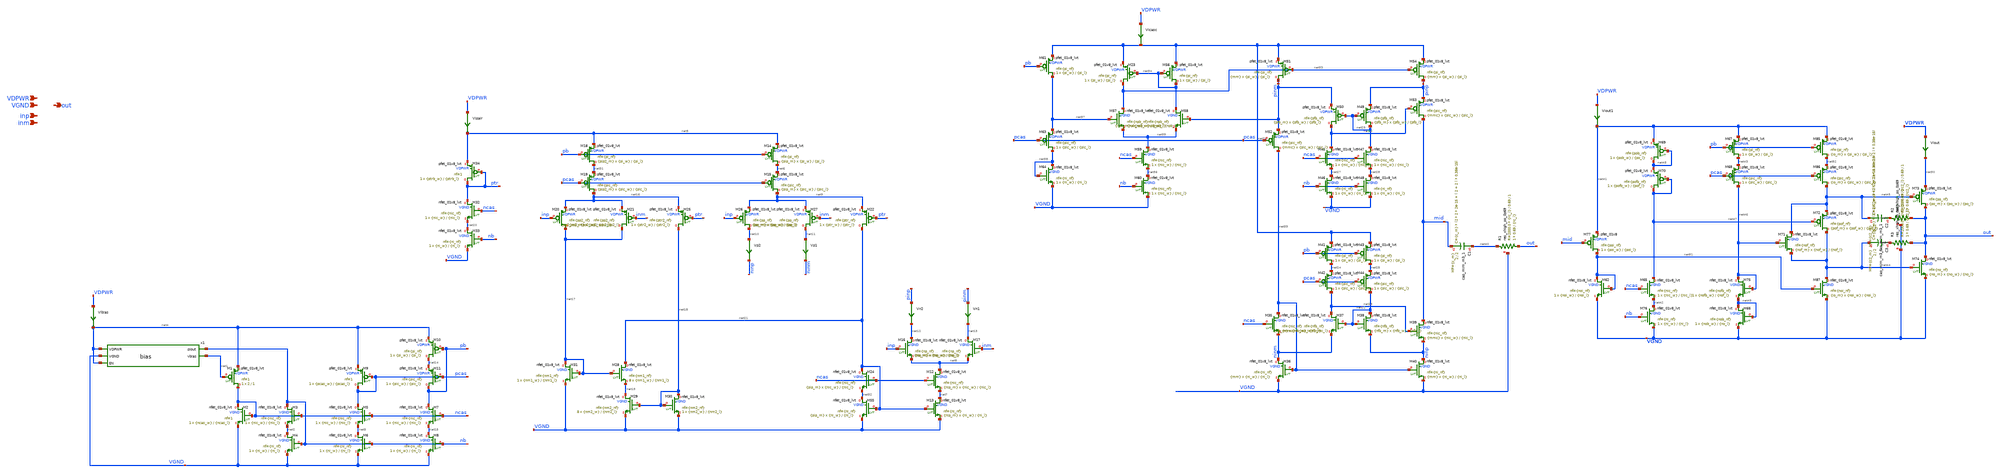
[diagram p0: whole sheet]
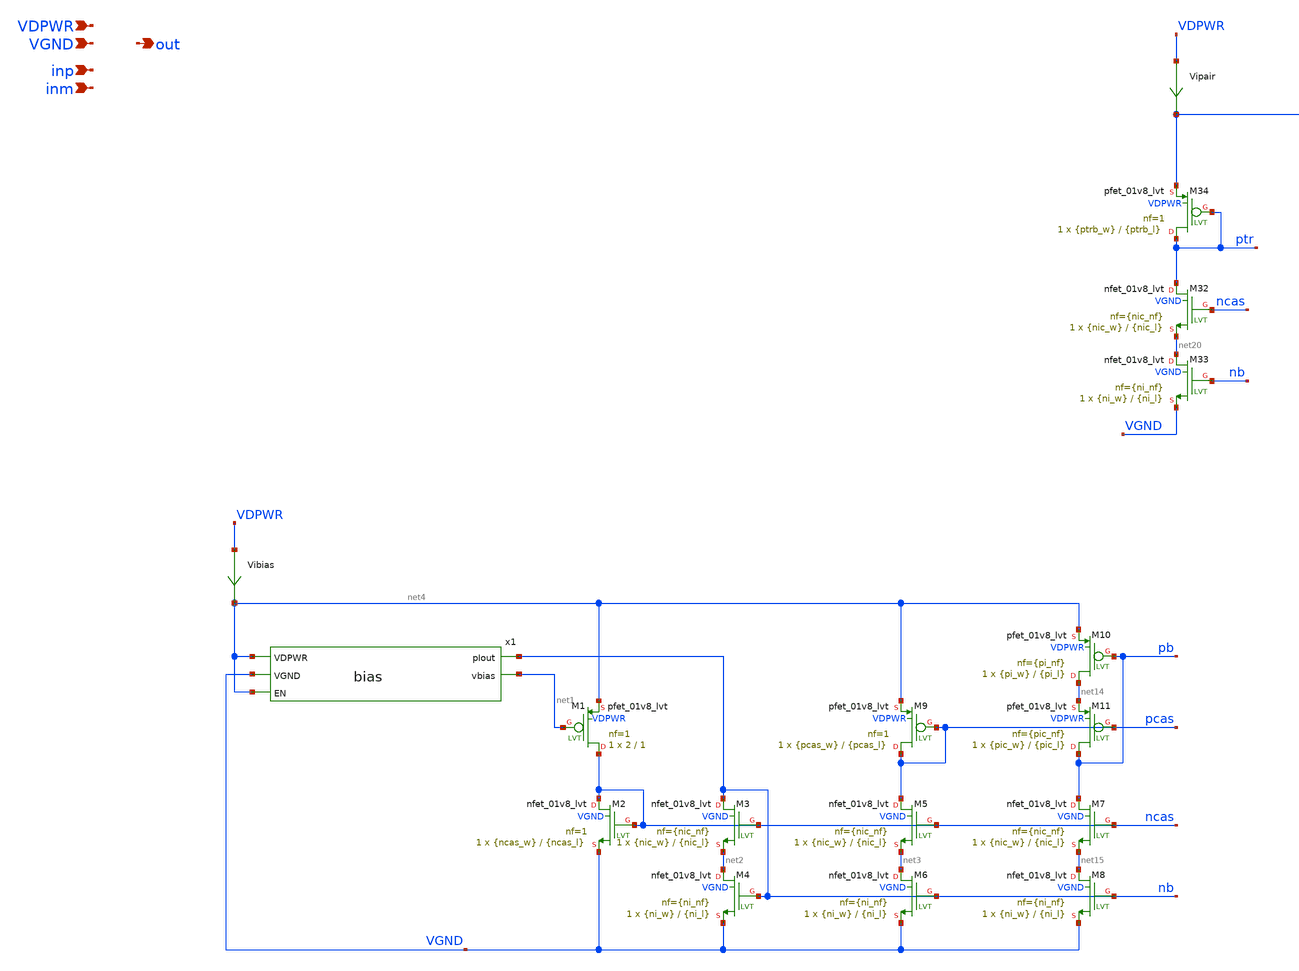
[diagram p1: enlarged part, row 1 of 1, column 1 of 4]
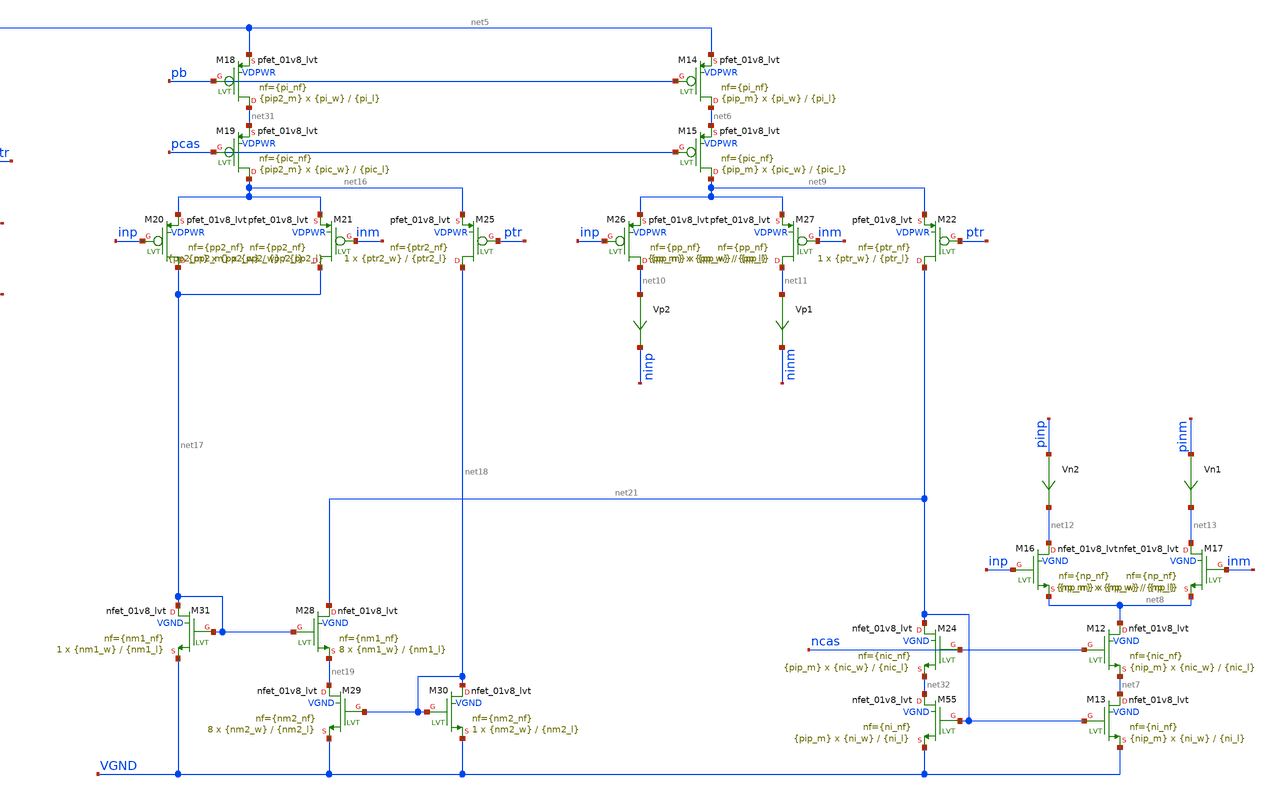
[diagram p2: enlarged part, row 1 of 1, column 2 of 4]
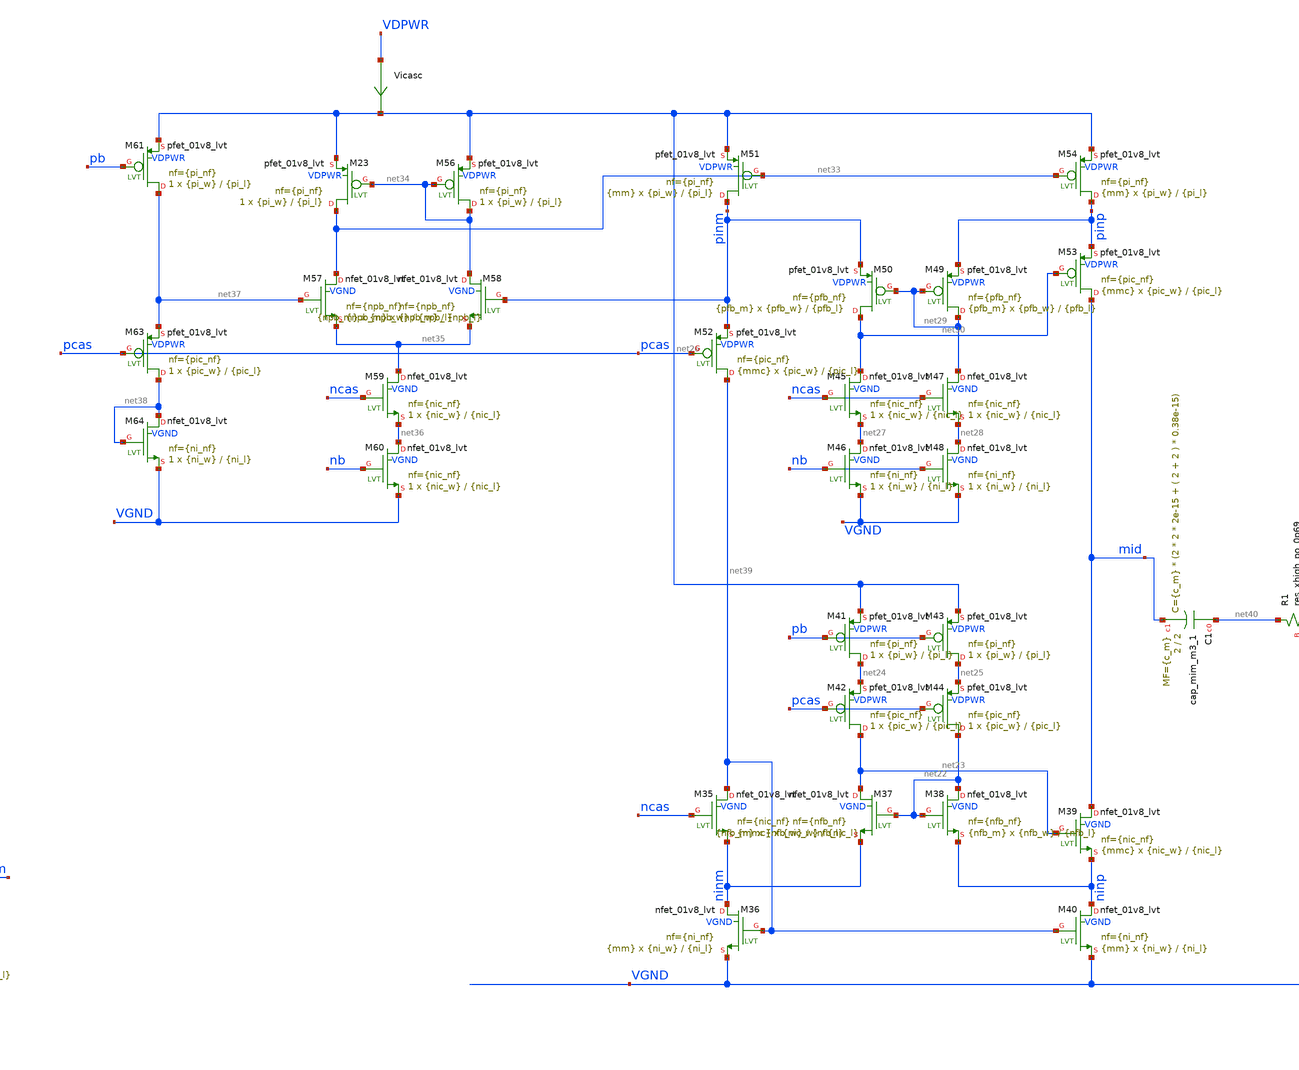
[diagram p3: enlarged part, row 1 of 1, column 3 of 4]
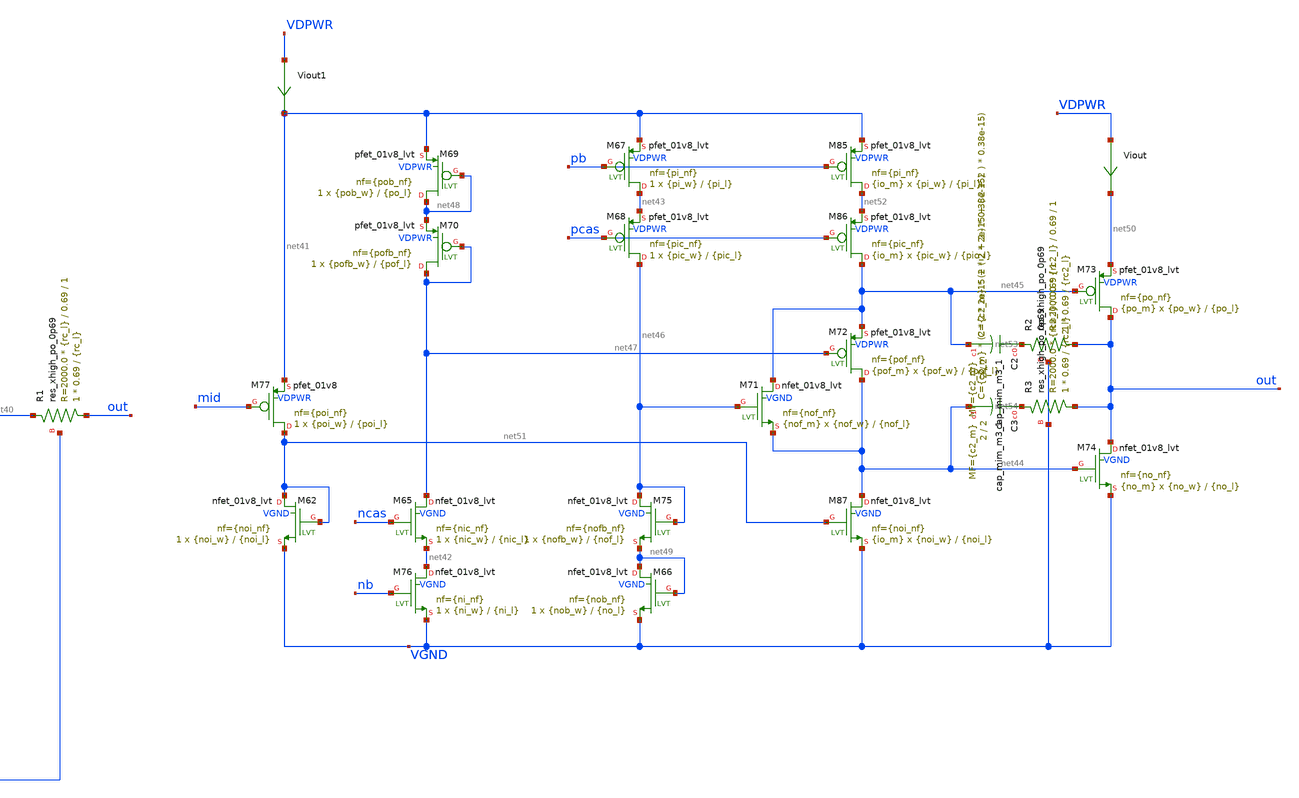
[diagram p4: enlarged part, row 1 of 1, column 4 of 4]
** sch_path: xschem/opamp_testing2.sch
**.subckt opamp_testing2 VDPWR VGND inp inm out
*.ipin VDPWR
*.ipin VGND
*.ipin inp
*.ipin inm
*.opin out
x1 net4 nb VGND net4 net1 bias
XM1 ncas net1 net4 VDPWR sky130_fd_pr__pfet_01v8_lvt L=1 W=2 nf=1 ad='int((1 + 1)/2) * 2 / 1 * 0.29'
+ as='int((1 + 2)/2) * 2 / 1 * 0.29' pd='2*int((1 + 1)/2) * (2 / 1 + 0.29)' ps='2*int((1 + 2)/2) * (2 / 1 + 0.29)'
+ nrd='0.29 / 2 ' nrs='0.29 / 2 ' sa=0 sb=0 sd=0 mult=1 m=1
XM2 ncas ncas VGND VGND sky130_fd_pr__nfet_01v8_lvt L={ncas_l} W={ncas_w} nf=1 ad='int((1 + 1)/2) * {ncas_w} / 1 * 0.29'
+ as='int((1 + 2)/2) * {ncas_w} / 1 * 0.29' pd='2*int((1 + 1)/2) * ({ncas_w} / 1 + 0.29)' ps='2*int((1 + 2)/2) * ({ncas_w} / 1 + 0.29)'
+ nrd='0.29 / {ncas_w} ' nrs='0.29 / {ncas_w} ' sa=0 sb=0 sd=0 mult=1 m=1
XM3 nb ncas net2 VGND sky130_fd_pr__nfet_01v8_lvt L={nic_l} W={nic_w} nf={nic_nf} ad='int(({nic_nf} + 1)/2) * {nic_w} / {nic_nf} * 0.29'
+ as='int(({nic_nf} + 2)/2) * {nic_w} / {nic_nf} * 0.29' pd='2*int(({nic_nf} + 1)/2) * ({nic_w} / {nic_nf} + 0.29)'
+ ps='2*int(({nic_nf} + 2)/2) * ({nic_w} / {nic_nf} + 0.29)' nrd='0.29 / {nic_w} ' nrs='0.29 / {nic_w} '
+ sa=0 sb=0 sd=0 mult=1 m=1
XM4 net2 nb VGND VGND sky130_fd_pr__nfet_01v8_lvt L={ni_l} W={ni_w} nf={ni_nf} ad='int(({ni_nf} + 1)/2) * {ni_w} / {ni_nf} * 0.29'
+ as='int(({ni_nf} + 2)/2) * {ni_w} / {ni_nf} * 0.29' pd='2*int(({ni_nf} + 1)/2) * ({ni_w} / {ni_nf} + 0.29)'
+ ps='2*int(({ni_nf} + 2)/2) * ({ni_w} / {ni_nf} + 0.29)' nrd='0.29 / {ni_w} ' nrs='0.29 / {ni_w} ' sa=0
+ sb=0 sd=0 mult=1 m=1
XM5 pcas ncas net3 VGND sky130_fd_pr__nfet_01v8_lvt L={nic_l} W={nic_w} nf={nic_nf} ad='int(({nic_nf} + 1)/2) * {nic_w} / {nic_nf} * 0.29'
+ as='int(({nic_nf} + 2)/2) * {nic_w} / {nic_nf} * 0.29' pd='2*int(({nic_nf} + 1)/2) * ({nic_w} / {nic_nf} + 0.29)'
+ ps='2*int(({nic_nf} + 2)/2) * ({nic_w} / {nic_nf} + 0.29)' nrd='0.29 / {nic_w} ' nrs='0.29 / {nic_w} '
+ sa=0 sb=0 sd=0 mult=1 m=1
XM6 net3 nb VGND VGND sky130_fd_pr__nfet_01v8_lvt L={ni_l} W={ni_w} nf={ni_nf} ad='int(({ni_nf} + 1)/2) * {ni_w} / {ni_nf} * 0.29'
+ as='int(({ni_nf} + 2)/2) * {ni_w} / {ni_nf} * 0.29' pd='2*int(({ni_nf} + 1)/2) * ({ni_w} / {ni_nf} + 0.29)'
+ ps='2*int(({ni_nf} + 2)/2) * ({ni_w} / {ni_nf} + 0.29)' nrd='0.29 / {ni_w} ' nrs='0.29 / {ni_w} ' sa=0
+ sb=0 sd=0 mult=1 m=1
XM7 pb ncas net15 VGND sky130_fd_pr__nfet_01v8_lvt L={nic_l} W={nic_w} nf={nic_nf} ad='int(({nic_nf} + 1)/2) * {nic_w} / {nic_nf} * 0.29'
+ as='int(({nic_nf} + 2)/2) * {nic_w} / {nic_nf} * 0.29' pd='2*int(({nic_nf} + 1)/2) * ({nic_w} / {nic_nf} + 0.29)'
+ ps='2*int(({nic_nf} + 2)/2) * ({nic_w} / {nic_nf} + 0.29)' nrd='0.29 / {nic_w} ' nrs='0.29 / {nic_w} '
+ sa=0 sb=0 sd=0 mult=1 m=1
XM8 net15 nb VGND VGND sky130_fd_pr__nfet_01v8_lvt L={ni_l} W={ni_w} nf={ni_nf} ad='int(({ni_nf} + 1)/2) * {ni_w} / {ni_nf} * 0.29'
+ as='int(({ni_nf} + 2)/2) * {ni_w} / {ni_nf} * 0.29' pd='2*int(({ni_nf} + 1)/2) * ({ni_w} / {ni_nf} + 0.29)'
+ ps='2*int(({ni_nf} + 2)/2) * ({ni_w} / {ni_nf} + 0.29)' nrd='0.29 / {ni_w} ' nrs='0.29 / {ni_w} ' sa=0
+ sb=0 sd=0 mult=1 m=1
XM9 pcas pcas net4 VDPWR sky130_fd_pr__pfet_01v8_lvt L={pcas_l} W={pcas_w} nf=1 ad='int((1 + 1)/2) * {pcas_w} / 1 * 0.29'
+ as='int((1 + 2)/2) * {pcas_w} / 1 * 0.29' pd='2*int((1 + 1)/2) * ({pcas_w} / 1 + 0.29)' ps='2*int((1 + 2)/2) * ({pcas_w} / 1 + 0.29)'
+ nrd='0.29 / {pcas_w} ' nrs='0.29 / {pcas_w} ' sa=0 sb=0 sd=0 mult=1 m=1
XM10 net14 pb net4 VDPWR sky130_fd_pr__pfet_01v8_lvt L={pi_l} W={pi_w} nf={pi_nf} ad='int(({pi_nf} + 1)/2) * {pi_w} / {pi_nf} * 0.29'
+ as='int(({pi_nf} + 2)/2) * {pi_w} / {pi_nf} * 0.29' pd='2*int(({pi_nf} + 1)/2) * ({pi_w} / {pi_nf} + 0.29)'
+ ps='2*int(({pi_nf} + 2)/2) * ({pi_w} / {pi_nf} + 0.29)' nrd='0.29 / {pi_w} ' nrs='0.29 / {pi_w} ' sa=0
+ sb=0 sd=0 mult=1 m=1
XM11 pb pcas net14 VDPWR sky130_fd_pr__pfet_01v8_lvt L={pic_l} W={pic_w} nf={pic_nf} ad='int(({pic_nf} + 1)/2) * {pic_w} / {pic_nf} * 0.29'
+ as='int(({pic_nf} + 2)/2) * {pic_w} / {pic_nf} * 0.29' pd='2*int(({pic_nf} + 1)/2) * ({pic_w} / {pic_nf} + 0.29)'
+ ps='2*int(({pic_nf} + 2)/2) * ({pic_w} / {pic_nf} + 0.29)' nrd='0.29 / {pic_w} ' nrs='0.29 / {pic_w} '
+ sa=0 sb=0 sd=0 mult=1 m=1
XM12 net8 ncas net7 VGND sky130_fd_pr__nfet_01v8_lvt L={nic_l} W={nic_w} nf={nic_nf} ad='int(({nic_nf} + 1)/2) * {nic_w} / {nic_nf} * 0.29'
+ as='int(({nic_nf} + 2)/2) * {nic_w} / {nic_nf} * 0.29' pd='2*int(({nic_nf} + 1)/2) * ({nic_w} / {nic_nf} + 0.29)'
+ ps='2*int(({nic_nf} + 2)/2) * ({nic_w} / {nic_nf} + 0.29)' nrd='0.29 / {nic_w} ' nrs='0.29 / {nic_w} '
+ sa=0 sb=0 sd=0 mult={nip_m} m={nip_m}
XM13 net7 net21 VGND VGND sky130_fd_pr__nfet_01v8_lvt L={ni_l} W={ni_w} nf={ni_nf} ad='int(({ni_nf} + 1)/2) * {ni_w} / {ni_nf} * 0.29'
+ as='int(({ni_nf} + 2)/2) * {ni_w} / {ni_nf} * 0.29' pd='2*int(({ni_nf} + 1)/2) * ({ni_w} / {ni_nf} + 0.29)'
+ ps='2*int(({ni_nf} + 2)/2) * ({ni_w} / {ni_nf} + 0.29)' nrd='0.29 / {ni_w} ' nrs='0.29 / {ni_w} ' sa=0
+ sb=0 sd=0 mult={nip_m} m={nip_m}
XM14 net6 pb net5 VDPWR sky130_fd_pr__pfet_01v8_lvt L={pi_l} W={pi_w} nf={pi_nf} ad='int(({pi_nf} + 1)/2) * {pi_w} / {pi_nf} * 0.29'
+ as='int(({pi_nf} + 2)/2) * {pi_w} / {pi_nf} * 0.29' pd='2*int(({pi_nf} + 1)/2) * ({pi_w} / {pi_nf} + 0.29)'
+ ps='2*int(({pi_nf} + 2)/2) * ({pi_w} / {pi_nf} + 0.29)' nrd='0.29 / {pi_w} ' nrs='0.29 / {pi_w} ' sa=0
+ sb=0 sd=0 mult={pip_m} m={pip_m}
XM15 net9 pcas net6 VDPWR sky130_fd_pr__pfet_01v8_lvt L={pic_l} W={pic_w} nf={pic_nf} ad='int(({pic_nf} + 1)/2) * {pic_w} / {pic_nf} * 0.29'
+ as='int(({pic_nf} + 2)/2) * {pic_w} / {pic_nf} * 0.29' pd='2*int(({pic_nf} + 1)/2) * ({pic_w} / {pic_nf} + 0.29)'
+ ps='2*int(({pic_nf} + 2)/2) * ({pic_w} / {pic_nf} + 0.29)' nrd='0.29 / {pic_w} ' nrs='0.29 / {pic_w} '
+ sa=0 sb=0 sd=0 mult={pip_m} m={pip_m}
XM16 net12 inp net8 VGND sky130_fd_pr__nfet_01v8_lvt L={np_l} W={np_w} nf={np_nf} ad='int(({np_nf} + 1)/2) * {np_w} / {np_nf} * 0.29'
+ as='int(({np_nf} + 2)/2) * {np_w} / {np_nf} * 0.29' pd='2*int(({np_nf} + 1)/2) * ({np_w} / {np_nf} + 0.29)'
+ ps='2*int(({np_nf} + 2)/2) * ({np_w} / {np_nf} + 0.29)' nrd='0.29 / {np_w} ' nrs='0.29 / {np_w} ' sa=0
+ sb=0 sd=0 mult={np_m} m={np_m}
XM17 net13 inm net8 VGND sky130_fd_pr__nfet_01v8_lvt L={np_l} W={np_w} nf={np_nf} ad='int(({np_nf} + 1)/2) * {np_w} / {np_nf} * 0.29'
+ as='int(({np_nf} + 2)/2) * {np_w} / {np_nf} * 0.29' pd='2*int(({np_nf} + 1)/2) * ({np_w} / {np_nf} + 0.29)'
+ ps='2*int(({np_nf} + 2)/2) * ({np_w} / {np_nf} + 0.29)' nrd='0.29 / {np_w} ' nrs='0.29 / {np_w} ' sa=0
+ sb=0 sd=0 mult={np_m} m={np_m}
XM26 net10 inp net9 VDPWR sky130_fd_pr__pfet_01v8_lvt L={pp_l} W={pp_w} nf={pp_nf} ad='int(({pp_nf} + 1)/2) * {pp_w} / {pp_nf} * 0.29'
+ as='int(({pp_nf} + 2)/2) * {pp_w} / {pp_nf} * 0.29' pd='2*int(({pp_nf} + 1)/2) * ({pp_w} / {pp_nf} + 0.29)'
+ ps='2*int(({pp_nf} + 2)/2) * ({pp_w} / {pp_nf} + 0.29)' nrd='0.29 / {pp_w} ' nrs='0.29 / {pp_w} ' sa=0
+ sb=0 sd=0 mult={pp_m} m={pp_m}
XM27 net11 inm net9 VDPWR sky130_fd_pr__pfet_01v8_lvt L={pp_l} W={pp_w} nf={pp_nf} ad='int(({pp_nf} + 1)/2) * {pp_w} / {pp_nf} * 0.29'
+ as='int(({pp_nf} + 2)/2) * {pp_w} / {pp_nf} * 0.29' pd='2*int(({pp_nf} + 1)/2) * ({pp_w} / {pp_nf} + 0.29)'
+ ps='2*int(({pp_nf} + 2)/2) * ({pp_w} / {pp_nf} + 0.29)' nrd='0.29 / {pp_w} ' nrs='0.29 / {pp_w} ' sa=0
+ sb=0 sd=0 mult={pp_m} m={pp_m}
Vp1 net11 ninm 0
.save i(vp1)
Vp2 net10 ninp 0
.save i(vp2)
Vn1 pinm net13 0
.save i(vn1)
Vn2 pinp net12 0
.save i(vn2)
XM18 net31 pb net5 VDPWR sky130_fd_pr__pfet_01v8_lvt L={pi_l} W={pi_w} nf={pi_nf} ad='int(({pi_nf} + 1)/2) * {pi_w} / {pi_nf} * 0.29'
+ as='int(({pi_nf} + 2)/2) * {pi_w} / {pi_nf} * 0.29' pd='2*int(({pi_nf} + 1)/2) * ({pi_w} / {pi_nf} + 0.29)'
+ ps='2*int(({pi_nf} + 2)/2) * ({pi_w} / {pi_nf} + 0.29)' nrd='0.29 / {pi_w} ' nrs='0.29 / {pi_w} ' sa=0
+ sb=0 sd=0 mult={pip2_m} m={pip2_m}
XM19 net16 pcas net31 VDPWR sky130_fd_pr__pfet_01v8_lvt L={pic_l} W={pic_w} nf={pic_nf} ad='int(({pic_nf} + 1)/2) * {pic_w} / {pic_nf} * 0.29'
+ as='int(({pic_nf} + 2)/2) * {pic_w} / {pic_nf} * 0.29' pd='2*int(({pic_nf} + 1)/2) * ({pic_w} / {pic_nf} + 0.29)'
+ ps='2*int(({pic_nf} + 2)/2) * ({pic_w} / {pic_nf} + 0.29)' nrd='0.29 / {pic_w} ' nrs='0.29 / {pic_w} '
+ sa=0 sb=0 sd=0 mult={pip2_m} m={pip2_m}
XM20 net17 inp net16 VDPWR sky130_fd_pr__pfet_01v8_lvt L={pp2_l} W={pp2_w} nf={pp2_nf} ad='int(({pp2_nf} + 1)/2) * {pp2_w} / {pp2_nf} * 0.29'
+ as='int(({pp2_nf} + 2)/2) * {pp2_w} / {pp2_nf} * 0.29' pd='2*int(({pp2_nf} + 1)/2) * ({pp2_w} / {pp2_nf} + 0.29)'
+ ps='2*int(({pp2_nf} + 2)/2) * ({pp2_w} / {pp2_nf} + 0.29)' nrd='0.29 / {pp2_w} ' nrs='0.29 / {pp2_w} '
+ sa=0 sb=0 sd=0 mult={pp2_m} m={pp2_m}
XM21 net17 inm net16 VDPWR sky130_fd_pr__pfet_01v8_lvt L={pp2_l} W={pp2_w} nf={pp2_nf} ad='int(({pp2_nf} + 1)/2) * {pp2_w} / {pp2_nf} * 0.29'
+ as='int(({pp2_nf} + 2)/2) * {pp2_w} / {pp2_nf} * 0.29' pd='2*int(({pp2_nf} + 1)/2) * ({pp2_w} / {pp2_nf} + 0.29)'
+ ps='2*int(({pp2_nf} + 2)/2) * ({pp2_w} / {pp2_nf} + 0.29)' nrd='0.29 / {pp2_w} ' nrs='0.29 / {pp2_w} '
+ sa=0 sb=0 sd=0 mult={pp2_m} m={pp2_m}
XM25 net18 ptr net16 VDPWR sky130_fd_pr__pfet_01v8_lvt L={ptr2_l} W={ptr2_w} nf={ptr2_nf} ad='int(({ptr2_nf} + 1)/2) * {ptr2_w} / {ptr2_nf} * 0.29'
+ as='int(({ptr2_nf} + 2)/2) * {ptr2_w} / {ptr2_nf} * 0.29' pd='2*int(({ptr2_nf} + 1)/2) * ({ptr2_w} / {ptr2_nf} + 0.29)'
+ ps='2*int(({ptr2_nf} + 2)/2) * ({ptr2_w} / {ptr2_nf} + 0.29)' nrd='0.29 / {ptr2_w} ' nrs='0.29 / {ptr2_w} '
+ sa=0 sb=0 sd=0 mult=1 m=1
XM28 net21 net17 net19 VGND sky130_fd_pr__nfet_01v8_lvt L={nm1_l} W={nm1_w} nf={nm1_nf} ad='int(({nm1_nf} + 1)/2) * {nm1_w} / {nm1_nf} * 0.29'
+ as='int(({nm1_nf} + 2)/2) * {nm1_w} / {nm1_nf} * 0.29' pd='2*int(({nm1_nf} + 1)/2) * ({nm1_w} / {nm1_nf} + 0.29)'
+ ps='2*int(({nm1_nf} + 2)/2) * ({nm1_w} / {nm1_nf} + 0.29)' nrd='0.29 / {nm1_w} ' nrs='0.29 / {nm1_w} '
+ sa=0 sb=0 sd=0 mult=8 m=8
XM29 net19 net18 VGND VGND sky130_fd_pr__nfet_01v8_lvt L={nm2_l} W={nm2_w} nf={nm2_nf} ad='int(({nm2_nf} + 1)/2) * {nm2_w} / {nm2_nf} * 0.29'
+ as='int(({nm2_nf} + 2)/2) * {nm2_w} / {nm2_nf} * 0.29' pd='2*int(({nm2_nf} + 1)/2) * ({nm2_w} / {nm2_nf} + 0.29)'
+ ps='2*int(({nm2_nf} + 2)/2) * ({nm2_w} / {nm2_nf} + 0.29)' nrd='0.29 / {nm2_w} ' nrs='0.29 / {nm2_w} '
+ sa=0 sb=0 sd=0 mult=8 m=8
XM30 net18 net18 VGND VGND sky130_fd_pr__nfet_01v8_lvt L={nm2_l} W={nm2_w} nf={nm2_nf} ad='int(({nm2_nf} + 1)/2) * {nm2_w} / {nm2_nf} * 0.29'
+ as='int(({nm2_nf} + 2)/2) * {nm2_w} / {nm2_nf} * 0.29' pd='2*int(({nm2_nf} + 1)/2) * ({nm2_w} / {nm2_nf} + 0.29)'
+ ps='2*int(({nm2_nf} + 2)/2) * ({nm2_w} / {nm2_nf} + 0.29)' nrd='0.29 / {nm2_w} ' nrs='0.29 / {nm2_w} '
+ sa=0 sb=0 sd=0 mult=1 m=1
XM31 net17 net17 VGND VGND sky130_fd_pr__nfet_01v8_lvt L={nm1_l} W={nm1_w} nf={nm1_nf} ad='int(({nm1_nf} + 1)/2) * {nm1_w} / {nm1_nf} * 0.29'
+ as='int(({nm1_nf} + 2)/2) * {nm1_w} / {nm1_nf} * 0.29' pd='2*int(({nm1_nf} + 1)/2) * ({nm1_w} / {nm1_nf} + 0.29)'
+ ps='2*int(({nm1_nf} + 2)/2) * ({nm1_w} / {nm1_nf} + 0.29)' nrd='0.29 / {nm1_w} ' nrs='0.29 / {nm1_w} '
+ sa=0 sb=0 sd=0 mult=1 m=1
XM32 ptr ncas net20 VGND sky130_fd_pr__nfet_01v8_lvt L={nic_l} W={nic_w} nf={nic_nf} ad='int(({nic_nf} + 1)/2) * {nic_w} / {nic_nf} * 0.29'
+ as='int(({nic_nf} + 2)/2) * {nic_w} / {nic_nf} * 0.29' pd='2*int(({nic_nf} + 1)/2) * ({nic_w} / {nic_nf} + 0.29)'
+ ps='2*int(({nic_nf} + 2)/2) * ({nic_w} / {nic_nf} + 0.29)' nrd='0.29 / {nic_w} ' nrs='0.29 / {nic_w} '
+ sa=0 sb=0 sd=0 mult=1 m=1
XM33 net20 nb VGND VGND sky130_fd_pr__nfet_01v8_lvt L={ni_l} W={ni_w} nf={ni_nf} ad='int(({ni_nf} + 1)/2) * {ni_w} / {ni_nf} * 0.29'
+ as='int(({ni_nf} + 2)/2) * {ni_w} / {ni_nf} * 0.29' pd='2*int(({ni_nf} + 1)/2) * ({ni_w} / {ni_nf} + 0.29)'
+ ps='2*int(({ni_nf} + 2)/2) * ({ni_w} / {ni_nf} + 0.29)' nrd='0.29 / {ni_w} ' nrs='0.29 / {ni_w} ' sa=0
+ sb=0 sd=0 mult=1 m=1
XM34 ptr ptr net5 VDPWR sky130_fd_pr__pfet_01v8_lvt L={ptrb_l} W={ptrb_w} nf=1 ad='int((1 + 1)/2) * {ptrb_w} / 1 * 0.29'
+ as='int((1 + 2)/2) * {ptrb_w} / 1 * 0.29' pd='2*int((1 + 1)/2) * ({ptrb_w} / 1 + 0.29)' ps='2*int((1 + 2)/2) * ({ptrb_w} / 1 + 0.29)'
+ nrd='0.29 / {ptrb_w} ' nrs='0.29 / {ptrb_w} ' sa=0 sb=0 sd=0 mult=1 m=1
XM35 net39 ncas ninm VGND sky130_fd_pr__nfet_01v8_lvt L={nic_l} W={nic_w} nf={nic_nf} ad='int(({nic_nf} + 1)/2) * {nic_w} / {nic_nf} * 0.29'
+ as='int(({nic_nf} + 2)/2) * {nic_w} / {nic_nf} * 0.29' pd='2*int(({nic_nf} + 1)/2) * ({nic_w} / {nic_nf} + 0.29)'
+ ps='2*int(({nic_nf} + 2)/2) * ({nic_w} / {nic_nf} + 0.29)' nrd='0.29 / {nic_w} ' nrs='0.29 / {nic_w} '
+ sa=0 sb=0 sd=0 mult={mmc} m={mmc}
XM36 ninm net39 VGND VGND sky130_fd_pr__nfet_01v8_lvt L={ni_l} W={ni_w} nf={ni_nf} ad='int(({ni_nf} + 1)/2) * {ni_w} / {ni_nf} * 0.29'
+ as='int(({ni_nf} + 2)/2) * {ni_w} / {ni_nf} * 0.29' pd='2*int(({ni_nf} + 1)/2) * ({ni_w} / {ni_nf} + 0.29)'
+ ps='2*int(({ni_nf} + 2)/2) * ({ni_w} / {ni_nf} + 0.29)' nrd='0.29 / {ni_w} ' nrs='0.29 / {ni_w} ' sa=0
+ sb=0 sd=0 mult={mm} m={mm}
XM37 net23 net22 ninm VGND sky130_fd_pr__nfet_01v8_lvt L={nfb_l} W={nfb_w} nf={nfb_nf} ad='int(({nfb_nf} + 1)/2) * {nfb_w} / {nfb_nf} * 0.29'
+ as='int(({nfb_nf} + 2)/2) * {nfb_w} / {nfb_nf} * 0.29' pd='2*int(({nfb_nf} + 1)/2) * ({nfb_w} / {nfb_nf} + 0.29)'
+ ps='2*int(({nfb_nf} + 2)/2) * ({nfb_w} / {nfb_nf} + 0.29)' nrd='0.29 / {nfb_w} ' nrs='0.29 / {nfb_w} '
+ sa=0 sb=0 sd=0 mult={nfb_m} m={nfb_m}
XM39 mid net23 ninp VGND sky130_fd_pr__nfet_01v8_lvt L={nic_l} W={nic_w} nf={nic_nf} ad='int(({nic_nf} + 1)/2) * {nic_w} / {nic_nf} * 0.29'
+ as='int(({nic_nf} + 2)/2) * {nic_w} / {nic_nf} * 0.29' pd='2*int(({nic_nf} + 1)/2) * ({nic_w} / {nic_nf} + 0.29)'
+ ps='2*int(({nic_nf} + 2)/2) * ({nic_w} / {nic_nf} + 0.29)' nrd='0.29 / {nic_w} ' nrs='0.29 / {nic_w} '
+ sa=0 sb=0 sd=0 mult={mmc} m={mmc}
XM40 ninp net39 VGND VGND sky130_fd_pr__nfet_01v8_lvt L={ni_l} W={ni_w} nf={ni_nf} ad='int(({ni_nf} + 1)/2) * {ni_w} / {ni_nf} * 0.29'
+ as='int(({ni_nf} + 2)/2) * {ni_w} / {ni_nf} * 0.29' pd='2*int(({ni_nf} + 1)/2) * ({ni_w} / {ni_nf} + 0.29)'
+ ps='2*int(({ni_nf} + 2)/2) * ({ni_w} / {ni_nf} + 0.29)' nrd='0.29 / {ni_w} ' nrs='0.29 / {ni_w} ' sa=0
+ sb=0 sd=0 mult={mm} m={mm}
XM41 net24 pb net26 VDPWR sky130_fd_pr__pfet_01v8_lvt L={pi_l} W={pi_w} nf={pi_nf} ad='int(({pi_nf} + 1)/2) * {pi_w} / {pi_nf} * 0.29'
+ as='int(({pi_nf} + 2)/2) * {pi_w} / {pi_nf} * 0.29' pd='2*int(({pi_nf} + 1)/2) * ({pi_w} / {pi_nf} + 0.29)'
+ ps='2*int(({pi_nf} + 2)/2) * ({pi_w} / {pi_nf} + 0.29)' nrd='0.29 / {pi_w} ' nrs='0.29 / {pi_w} ' sa=0
+ sb=0 sd=0 mult=1 m=1
XM42 net23 pcas net24 VDPWR sky130_fd_pr__pfet_01v8_lvt L={pic_l} W={pic_w} nf={pic_nf} ad='int(({pic_nf} + 1)/2) * {pic_w} / {pic_nf} * 0.29'
+ as='int(({pic_nf} + 2)/2) * {pic_w} / {pic_nf} * 0.29' pd='2*int(({pic_nf} + 1)/2) * ({pic_w} / {pic_nf} + 0.29)'
+ ps='2*int(({pic_nf} + 2)/2) * ({pic_w} / {pic_nf} + 0.29)' nrd='0.29 / {pic_w} ' nrs='0.29 / {pic_w} '
+ sa=0 sb=0 sd=0 mult=1 m=1
XM43 net25 pb net26 VDPWR sky130_fd_pr__pfet_01v8_lvt L={pi_l} W={pi_w} nf={pi_nf} ad='int(({pi_nf} + 1)/2) * {pi_w} / {pi_nf} * 0.29'
+ as='int(({pi_nf} + 2)/2) * {pi_w} / {pi_nf} * 0.29' pd='2*int(({pi_nf} + 1)/2) * ({pi_w} / {pi_nf} + 0.29)'
+ ps='2*int(({pi_nf} + 2)/2) * ({pi_w} / {pi_nf} + 0.29)' nrd='0.29 / {pi_w} ' nrs='0.29 / {pi_w} ' sa=0
+ sb=0 sd=0 mult=1 m=1
XM44 net22 pcas net25 VDPWR sky130_fd_pr__pfet_01v8_lvt L={pic_l} W={pic_w} nf={pic_nf} ad='int(({pic_nf} + 1)/2) * {pic_w} / {pic_nf} * 0.29'
+ as='int(({pic_nf} + 2)/2) * {pic_w} / {pic_nf} * 0.29' pd='2*int(({pic_nf} + 1)/2) * ({pic_w} / {pic_nf} + 0.29)'
+ ps='2*int(({pic_nf} + 2)/2) * ({pic_w} / {pic_nf} + 0.29)' nrd='0.29 / {pic_w} ' nrs='0.29 / {pic_w} '
+ sa=0 sb=0 sd=0 mult=1 m=1
XM45 net30 ncas net27 VGND sky130_fd_pr__nfet_01v8_lvt L={nic_l} W={nic_w} nf={nic_nf} ad='int(({nic_nf} + 1)/2) * {nic_w} / {nic_nf} * 0.29'
+ as='int(({nic_nf} + 2)/2) * {nic_w} / {nic_nf} * 0.29' pd='2*int(({nic_nf} + 1)/2) * ({nic_w} / {nic_nf} + 0.29)'
+ ps='2*int(({nic_nf} + 2)/2) * ({nic_w} / {nic_nf} + 0.29)' nrd='0.29 / {nic_w} ' nrs='0.29 / {nic_w} '
+ sa=0 sb=0 sd=0 mult=1 m=1
XM46 net27 nb VGND VGND sky130_fd_pr__nfet_01v8_lvt L={ni_l} W={ni_w} nf={ni_nf} ad='int(({ni_nf} + 1)/2) * {ni_w} / {ni_nf} * 0.29'
+ as='int(({ni_nf} + 2)/2) * {ni_w} / {ni_nf} * 0.29' pd='2*int(({ni_nf} + 1)/2) * ({ni_w} / {ni_nf} + 0.29)'
+ ps='2*int(({ni_nf} + 2)/2) * ({ni_w} / {ni_nf} + 0.29)' nrd='0.29 / {ni_w} ' nrs='0.29 / {ni_w} ' sa=0
+ sb=0 sd=0 mult=1 m=1
XM47 net29 ncas net28 VGND sky130_fd_pr__nfet_01v8_lvt L={nic_l} W={nic_w} nf={nic_nf} ad='int(({nic_nf} + 1)/2) * {nic_w} / {nic_nf} * 0.29'
+ as='int(({nic_nf} + 2)/2) * {nic_w} / {nic_nf} * 0.29' pd='2*int(({nic_nf} + 1)/2) * ({nic_w} / {nic_nf} + 0.29)'
+ ps='2*int(({nic_nf} + 2)/2) * ({nic_w} / {nic_nf} + 0.29)' nrd='0.29 / {nic_w} ' nrs='0.29 / {nic_w} '
+ sa=0 sb=0 sd=0 mult=1 m=1
XM48 net28 nb VGND VGND sky130_fd_pr__nfet_01v8_lvt L={ni_l} W={ni_w} nf={ni_nf} ad='int(({ni_nf} + 1)/2) * {ni_w} / {ni_nf} * 0.29'
+ as='int(({ni_nf} + 2)/2) * {ni_w} / {ni_nf} * 0.29' pd='2*int(({ni_nf} + 1)/2) * ({ni_w} / {ni_nf} + 0.29)'
+ ps='2*int(({ni_nf} + 2)/2) * ({ni_w} / {ni_nf} + 0.29)' nrd='0.29 / {ni_w} ' nrs='0.29 / {ni_w} ' sa=0
+ sb=0 sd=0 mult=1 m=1
XM50 net30 net29 pinm VDPWR sky130_fd_pr__pfet_01v8_lvt L={pfb_l} W={pfb_w} nf={pfb_nf} ad='int(({pfb_nf} + 1)/2) * {pfb_w} / {pfb_nf} * 0.29'
+ as='int(({pfb_nf} + 2)/2) * {pfb_w} / {pfb_nf} * 0.29' pd='2*int(({pfb_nf} + 1)/2) * ({pfb_w} / {pfb_nf} + 0.29)'
+ ps='2*int(({pfb_nf} + 2)/2) * ({pfb_w} / {pfb_nf} + 0.29)' nrd='0.29 / {pfb_w} ' nrs='0.29 / {pfb_w} '
+ sa=0 sb=0 sd=0 mult={pfb_m} m={pfb_m}
XM51 pinm net33 net26 VDPWR sky130_fd_pr__pfet_01v8_lvt L={pi_l} W={pi_w} nf={pi_nf} ad='int(({pi_nf} + 1)/2) * {pi_w} / {pi_nf} * 0.29'
+ as='int(({pi_nf} + 2)/2) * {pi_w} / {pi_nf} * 0.29' pd='2*int(({pi_nf} + 1)/2) * ({pi_w} / {pi_nf} + 0.29)'
+ ps='2*int(({pi_nf} + 2)/2) * ({pi_w} / {pi_nf} + 0.29)' nrd='0.29 / {pi_w} ' nrs='0.29 / {pi_w} ' sa=0
+ sb=0 sd=0 mult={mm} m={mm}
XM52 net39 pcas pinm VDPWR sky130_fd_pr__pfet_01v8_lvt L={pic_l} W={pic_w} nf={pic_nf} ad='int(({pic_nf} + 1)/2) * {pic_w} / {pic_nf} * 0.29'
+ as='int(({pic_nf} + 2)/2) * {pic_w} / {pic_nf} * 0.29' pd='2*int(({pic_nf} + 1)/2) * ({pic_w} / {pic_nf} + 0.29)'
+ ps='2*int(({pic_nf} + 2)/2) * ({pic_w} / {pic_nf} + 0.29)' nrd='0.29 / {pic_w} ' nrs='0.29 / {pic_w} '
+ sa=0 sb=0 sd=0 mult={mmc} m={mmc}
XM53 mid net30 pinp VDPWR sky130_fd_pr__pfet_01v8_lvt L={pic_l} W={pic_w} nf={pic_nf} ad='int(({pic_nf} + 1)/2) * {pic_w} / {pic_nf} * 0.29'
+ as='int(({pic_nf} + 2)/2) * {pic_w} / {pic_nf} * 0.29' pd='2*int(({pic_nf} + 1)/2) * ({pic_w} / {pic_nf} + 0.29)'
+ ps='2*int(({pic_nf} + 2)/2) * ({pic_w} / {pic_nf} + 0.29)' nrd='0.29 / {pic_w} ' nrs='0.29 / {pic_w} '
+ sa=0 sb=0 sd=0 mult={mmc} m={mmc}
XM54 pinp net33 net26 VDPWR sky130_fd_pr__pfet_01v8_lvt L={pi_l} W={pi_w} nf={pi_nf} ad='int(({pi_nf} + 1)/2) * {pi_w} / {pi_nf} * 0.29'
+ as='int(({pi_nf} + 2)/2) * {pi_w} / {pi_nf} * 0.29' pd='2*int(({pi_nf} + 1)/2) * ({pi_w} / {pi_nf} + 0.29)'
+ ps='2*int(({pi_nf} + 2)/2) * ({pi_w} / {pi_nf} + 0.29)' nrd='0.29 / {pi_w} ' nrs='0.29 / {pi_w} ' sa=0
+ sb=0 sd=0 mult={mm} m={mm}
Vibias VDPWR net4 0
.save i(vibias)
Vipair VDPWR net5 0
.save i(vipair)
Vicasc VDPWR net26 0
.save i(vicasc)
XM49 net29 net29 pinp VDPWR sky130_fd_pr__pfet_01v8_lvt L={pfb_l} W={pfb_w} nf={pfb_nf} ad='int(({pfb_nf} + 1)/2) * {pfb_w} / {pfb_nf} * 0.29'
+ as='int(({pfb_nf} + 2)/2) * {pfb_w} / {pfb_nf} * 0.29' pd='2*int(({pfb_nf} + 1)/2) * ({pfb_w} / {pfb_nf} + 0.29)'
+ ps='2*int(({pfb_nf} + 2)/2) * ({pfb_w} / {pfb_nf} + 0.29)' nrd='0.29 / {pfb_w} ' nrs='0.29 / {pfb_w} '
+ sa=0 sb=0 sd=0 mult={pfb_m} m={pfb_m}
XM38 net22 net22 ninp VGND sky130_fd_pr__nfet_01v8_lvt L={nfb_l} W={nfb_w} nf={nfb_nf} ad='int(({nfb_nf} + 1)/2) * {nfb_w} / {nfb_nf} * 0.29'
+ as='int(({nfb_nf} + 2)/2) * {nfb_w} / {nfb_nf} * 0.29' pd='2*int(({nfb_nf} + 1)/2) * ({nfb_w} / {nfb_nf} + 0.29)'
+ ps='2*int(({nfb_nf} + 2)/2) * ({nfb_w} / {nfb_nf} + 0.29)' nrd='0.29 / {nfb_w} ' nrs='0.29 / {nfb_w} '
+ sa=0 sb=0 sd=0 mult={nfb_m} m={nfb_m}
XM24 net21 ncas net32 VGND sky130_fd_pr__nfet_01v8_lvt L={nic_l} W={nic_w} nf={nic_nf} ad='int(({nic_nf} + 1)/2) * {nic_w} / {nic_nf} * 0.29'
+ as='int(({nic_nf} + 2)/2) * {nic_w} / {nic_nf} * 0.29' pd='2*int(({nic_nf} + 1)/2) * ({nic_w} / {nic_nf} + 0.29)'
+ ps='2*int(({nic_nf} + 2)/2) * ({nic_w} / {nic_nf} + 0.29)' nrd='0.29 / {nic_w} ' nrs='0.29 / {nic_w} '
+ sa=0 sb=0 sd=0 mult={pip_m} m={pip_m}
XM55 net32 net21 VGND VGND sky130_fd_pr__nfet_01v8_lvt L={ni_l} W={ni_w} nf={ni_nf} ad='int(({ni_nf} + 1)/2) * {ni_w} / {ni_nf} * 0.29'
+ as='int(({ni_nf} + 2)/2) * {ni_w} / {ni_nf} * 0.29' pd='2*int(({ni_nf} + 1)/2) * ({ni_w} / {ni_nf} + 0.29)'
+ ps='2*int(({ni_nf} + 2)/2) * ({ni_w} / {ni_nf} + 0.29)' nrd='0.29 / {ni_w} ' nrs='0.29 / {ni_w} ' sa=0
+ sb=0 sd=0 mult={pip_m} m={pip_m}
XM22 net21 ptr net9 VDPWR sky130_fd_pr__pfet_01v8_lvt L={ptr_l} W={ptr_w} nf={ptr_nf} ad='int(({ptr_nf} + 1)/2) * {ptr_w} / {ptr_nf} * 0.29'
+ as='int(({ptr_nf} + 2)/2) * {ptr_w} / {ptr_nf} * 0.29' pd='2*int(({ptr_nf} + 1)/2) * ({ptr_w} / {ptr_nf} + 0.29)'
+ ps='2*int(({ptr_nf} + 2)/2) * ({ptr_w} / {ptr_nf} + 0.29)' nrd='0.29 / {ptr_w} ' nrs='0.29 / {ptr_w} '
+ sa=0 sb=0 sd=0 mult=1 m=1
XM23 net33 net34 net26 VDPWR sky130_fd_pr__pfet_01v8_lvt L={pi_l} W={pi_w} nf={pi_nf} ad='int(({pi_nf} + 1)/2) * {pi_w} / {pi_nf} * 0.29'
+ as='int(({pi_nf} + 2)/2) * {pi_w} / {pi_nf} * 0.29' pd='2*int(({pi_nf} + 1)/2) * ({pi_w} / {pi_nf} + 0.29)'
+ ps='2*int(({pi_nf} + 2)/2) * ({pi_w} / {pi_nf} + 0.29)' nrd='0.29 / {pi_w} ' nrs='0.29 / {pi_w} ' sa=0
+ sb=0 sd=0 mult=1 m=1
XM56 net34 net34 net26 VDPWR sky130_fd_pr__pfet_01v8_lvt L={pi_l} W={pi_w} nf={pi_nf} ad='int(({pi_nf} + 1)/2) * {pi_w} / {pi_nf} * 0.29'
+ as='int(({pi_nf} + 2)/2) * {pi_w} / {pi_nf} * 0.29' pd='2*int(({pi_nf} + 1)/2) * ({pi_w} / {pi_nf} + 0.29)'
+ ps='2*int(({pi_nf} + 2)/2) * ({pi_w} / {pi_nf} + 0.29)' nrd='0.29 / {pi_w} ' nrs='0.29 / {pi_w} ' sa=0
+ sb=0 sd=0 mult=1 m=1
XM57 net33 net37 net35 VGND sky130_fd_pr__nfet_01v8_lvt L={npb_l} W={npb_w} nf={npb_nf} ad='int(({npb_nf} + 1)/2) * {npb_w} / {npb_nf} * 0.29'
+ as='int(({npb_nf} + 2)/2) * {npb_w} / {npb_nf} * 0.29' pd='2*int(({npb_nf} + 1)/2) * ({npb_w} / {npb_nf} + 0.29)'
+ ps='2*int(({npb_nf} + 2)/2) * ({npb_w} / {npb_nf} + 0.29)' nrd='0.29 / {npb_w} ' nrs='0.29 / {npb_w} '
+ sa=0 sb=0 sd=0 mult={npb_m} m={npb_m}
XM58 net34 pinm net35 VGND sky130_fd_pr__nfet_01v8_lvt L={npb_l} W={npb_w} nf={npb_nf} ad='int(({npb_nf} + 1)/2) * {npb_w} / {npb_nf} * 0.29'
+ as='int(({npb_nf} + 2)/2) * {npb_w} / {npb_nf} * 0.29' pd='2*int(({npb_nf} + 1)/2) * ({npb_w} / {npb_nf} + 0.29)'
+ ps='2*int(({npb_nf} + 2)/2) * ({npb_w} / {npb_nf} + 0.29)' nrd='0.29 / {npb_w} ' nrs='0.29 / {npb_w} '
+ sa=0 sb=0 sd=0 mult={npb_m} m={npb_m}
XM59 net35 ncas net36 VGND sky130_fd_pr__nfet_01v8_lvt L={nic_l} W={nic_w} nf={nic_nf} ad='int(({nic_nf} + 1)/2) * {nic_w} / {nic_nf} * 0.29'
+ as='int(({nic_nf} + 2)/2) * {nic_w} / {nic_nf} * 0.29' pd='2*int(({nic_nf} + 1)/2) * ({nic_w} / {nic_nf} + 0.29)'
+ ps='2*int(({nic_nf} + 2)/2) * ({nic_w} / {nic_nf} + 0.29)' nrd='0.29 / {nic_w} ' nrs='0.29 / {nic_w} '
+ sa=0 sb=0 sd=0 mult=1 m=1
XM60 net36 nb VGND VGND sky130_fd_pr__nfet_01v8_lvt L={nic_l} W={nic_w} nf={nic_nf} ad='int(({nic_nf} + 1)/2) * {nic_w} / {nic_nf} * 0.29'
+ as='int(({nic_nf} + 2)/2) * {nic_w} / {nic_nf} * 0.29' pd='2*int(({nic_nf} + 1)/2) * ({nic_w} / {nic_nf} + 0.29)'
+ ps='2*int(({nic_nf} + 2)/2) * ({nic_w} / {nic_nf} + 0.29)' nrd='0.29 / {nic_w} ' nrs='0.29 / {nic_w} '
+ sa=0 sb=0 sd=0 mult=1 m=1
XM61 net37 pb net26 VDPWR sky130_fd_pr__pfet_01v8_lvt L={pi_l} W={pi_w} nf={pi_nf} ad='int(({pi_nf} + 1)/2) * {pi_w} / {pi_nf} * 0.29'
+ as='int(({pi_nf} + 2)/2) * {pi_w} / {pi_nf} * 0.29' pd='2*int(({pi_nf} + 1)/2) * ({pi_w} / {pi_nf} + 0.29)'
+ ps='2*int(({pi_nf} + 2)/2) * ({pi_w} / {pi_nf} + 0.29)' nrd='0.29 / {pi_w} ' nrs='0.29 / {pi_w} ' sa=0
+ sb=0 sd=0 mult=1 m=1
XM63 net38 pcas net37 VDPWR sky130_fd_pr__pfet_01v8_lvt L={pic_l} W={pic_w} nf={pic_nf} ad='int(({pic_nf} + 1)/2) * {pic_w} / {pic_nf} * 0.29'
+ as='int(({pic_nf} + 2)/2) * {pic_w} / {pic_nf} * 0.29' pd='2*int(({pic_nf} + 1)/2) * ({pic_w} / {pic_nf} + 0.29)'
+ ps='2*int(({pic_nf} + 2)/2) * ({pic_w} / {pic_nf} + 0.29)' nrd='0.29 / {pic_w} ' nrs='0.29 / {pic_w} '
+ sa=0 sb=0 sd=0 mult=1 m=1
XM64 net38 net38 VGND VGND sky130_fd_pr__nfet_01v8_lvt L={ni_l} W={ni_w} nf={ni_nf} ad='int(({ni_nf} + 1)/2) * {ni_w} / {ni_nf} * 0.29'
+ as='int(({ni_nf} + 2)/2) * {ni_w} / {ni_nf} * 0.29' pd='2*int(({ni_nf} + 1)/2) * ({ni_w} / {ni_nf} + 0.29)'
+ ps='2*int(({ni_nf} + 2)/2) * ({ni_w} / {ni_nf} + 0.29)' nrd='0.29 / {ni_w} ' nrs='0.29 / {ni_w} ' sa=0
+ sb=0 sd=0 mult=1 m=1
XC1 net40 mid sky130_fd_pr__cap_mim_m3_1 W=2 L=2 MF={c_m} m={c_m}
XR1 out net40 VGND sky130_fd_pr__res_xhigh_po_0p69 L={rc_l} mult=1 m=1
XM65 net47 ncas net42 VGND sky130_fd_pr__nfet_01v8_lvt L={nic_l} W={nic_w} nf={nic_nf} ad='int(({nic_nf} + 1)/2) * {nic_w} / {nic_nf} * 0.29'
+ as='int(({nic_nf} + 2)/2) * {nic_w} / {nic_nf} * 0.29' pd='2*int(({nic_nf} + 1)/2) * ({nic_w} / {nic_nf} + 0.29)'
+ ps='2*int(({nic_nf} + 2)/2) * ({nic_w} / {nic_nf} + 0.29)' nrd='0.29 / {nic_w} ' nrs='0.29 / {nic_w} '
+ sa=0 sb=0 sd=0 mult=1 m=1
XM66 net49 net49 VGND VGND sky130_fd_pr__nfet_01v8_lvt L={no_l} W={nob_w} nf={nob_nf} ad='int(({nob_nf} + 1)/2) * {nob_w} / {nob_nf} * 0.29'
+ as='int(({nob_nf} + 2)/2) * {nob_w} / {nob_nf} * 0.29' pd='2*int(({nob_nf} + 1)/2) * ({nob_w} / {nob_nf} + 0.29)'
+ ps='2*int(({nob_nf} + 2)/2) * ({nob_w} / {nob_nf} + 0.29)' nrd='0.29 / {nob_w} ' nrs='0.29 / {nob_w} '
+ sa=0 sb=0 sd=0 mult=1 m=1
XM67 net43 pb net41 VDPWR sky130_fd_pr__pfet_01v8_lvt L={pi_l} W={pi_w} nf={pi_nf} ad='int(({pi_nf} + 1)/2) * {pi_w} / {pi_nf} * 0.29'
+ as='int(({pi_nf} + 2)/2) * {pi_w} / {pi_nf} * 0.29' pd='2*int(({pi_nf} + 1)/2) * ({pi_w} / {pi_nf} + 0.29)'
+ ps='2*int(({pi_nf} + 2)/2) * ({pi_w} / {pi_nf} + 0.29)' nrd='0.29 / {pi_w} ' nrs='0.29 / {pi_w} ' sa=0
+ sb=0 sd=0 mult=1 m=1
XM68 net46 pcas net43 VDPWR sky130_fd_pr__pfet_01v8_lvt L={pic_l} W={pic_w} nf={pic_nf} ad='int(({pic_nf} + 1)/2) * {pic_w} / {pic_nf} * 0.29'
+ as='int(({pic_nf} + 2)/2) * {pic_w} / {pic_nf} * 0.29' pd='2*int(({pic_nf} + 1)/2) * ({pic_w} / {pic_nf} + 0.29)'
+ ps='2*int(({pic_nf} + 2)/2) * ({pic_w} / {pic_nf} + 0.29)' nrd='0.29 / {pic_w} ' nrs='0.29 / {pic_w} '
+ sa=0 sb=0 sd=0 mult=1 m=1
XM69 net48 net48 net41 VDPWR sky130_fd_pr__pfet_01v8_lvt L={po_l} W={pob_w} nf={pob_nf} ad='int(({pob_nf} + 1)/2) * {pob_w} / {pob_nf} * 0.29'
+ as='int(({pob_nf} + 2)/2) * {pob_w} / {pob_nf} * 0.29' pd='2*int(({pob_nf} + 1)/2) * ({pob_w} / {pob_nf} + 0.29)'
+ ps='2*int(({pob_nf} + 2)/2) * ({pob_w} / {pob_nf} + 0.29)' nrd='0.29 / {pob_w} ' nrs='0.29 / {pob_w} '
+ sa=0 sb=0 sd=0 mult=1 m=1
XM70 net47 net47 net48 VDPWR sky130_fd_pr__pfet_01v8_lvt L={pof_l} W={pofb_w} nf={pofb_nf} ad='int(({pofb_nf} + 1)/2) * {pofb_w} / {pofb_nf} * 0.29'
+ as='int(({pofb_nf} + 2)/2) * {pofb_w} / {pofb_nf} * 0.29' pd='2*int(({pofb_nf} + 1)/2) * ({pofb_w} / {pofb_nf} + 0.29)'
+ ps='2*int(({pofb_nf} + 2)/2) * ({pofb_w} / {pofb_nf} + 0.29)' nrd='0.29 / {pofb_w} ' nrs='0.29 / {pofb_w} '
+ sa=0 sb=0 sd=0 mult=1 m=1
XM71 net45 net46 net44 VGND sky130_fd_pr__nfet_01v8_lvt L={nof_l} W={nof_w} nf={nof_nf} ad='int(({nof_nf} + 1)/2) * {nof_w} / {nof_nf} * 0.29'
+ as='int(({nof_nf} + 2)/2) * {nof_w} / {nof_nf} * 0.29' pd='2*int(({nof_nf} + 1)/2) * ({nof_w} / {nof_nf} + 0.29)'
+ ps='2*int(({nof_nf} + 2)/2) * ({nof_w} / {nof_nf} + 0.29)' nrd='0.29 / {nof_w} ' nrs='0.29 / {nof_w} '
+ sa=0 sb=0 sd=0 mult={nof_m} m={nof_m}
XM72 net44 net47 net45 VDPWR sky130_fd_pr__pfet_01v8_lvt L={pof_l} W={pof_w} nf={pof_nf} ad='int(({pof_nf} + 1)/2) * {pof_w} / {pof_nf} * 0.29'
+ as='int(({pof_nf} + 2)/2) * {pof_w} / {pof_nf} * 0.29' pd='2*int(({pof_nf} + 1)/2) * ({pof_w} / {pof_nf} + 0.29)'
+ ps='2*int(({pof_nf} + 2)/2) * ({pof_w} / {pof_nf} + 0.29)' nrd='0.29 / {pof_w} ' nrs='0.29 / {pof_w} '
+ sa=0 sb=0 sd=0 mult={pof_m} m={pof_m}
Viout VDPWR net50 0
.save i(viout)
XM73 out net45 net50 VDPWR sky130_fd_pr__pfet_01v8_lvt L={po_l} W={po_w} nf={po_nf} ad='int(({po_nf} + 1)/2) * {po_w} / {po_nf} * 0.29'
+ as='int(({po_nf} + 2)/2) * {po_w} / {po_nf} * 0.29' pd='2*int(({po_nf} + 1)/2) * ({po_w} / {po_nf} + 0.29)'
+ ps='2*int(({po_nf} + 2)/2) * ({po_w} / {po_nf} + 0.29)' nrd='0.29 / {po_w} ' nrs='0.29 / {po_w} ' sa=0
+ sb=0 sd=0 mult={po_m} m={po_m}
XM74 out net44 VGND VGND sky130_fd_pr__nfet_01v8_lvt L={no_l} W={no_w} nf={no_nf} ad='int(({no_nf} + 1)/2) * {no_w} / {no_nf} * 0.29'
+ as='int(({no_nf} + 2)/2) * {no_w} / {no_nf} * 0.29' pd='2*int(({no_nf} + 1)/2) * ({no_w} / {no_nf} + 0.29)'
+ ps='2*int(({no_nf} + 2)/2) * ({no_w} / {no_nf} + 0.29)' nrd='0.29 / {no_w} ' nrs='0.29 / {no_w} ' sa=0
+ sb=0 sd=0 mult={no_m} m={no_m}
XM75 net46 net46 net49 VGND sky130_fd_pr__nfet_01v8_lvt L={nof_l} W={nofb_w} nf={nofb_nf} ad='int(({nofb_nf} + 1)/2) * {nofb_w} / {nofb_nf} * 0.29'
+ as='int(({nofb_nf} + 2)/2) * {nofb_w} / {nofb_nf} * 0.29' pd='2*int(({nofb_nf} + 1)/2) * ({nofb_w} / {nofb_nf} + 0.29)'
+ ps='2*int(({nofb_nf} + 2)/2) * ({nofb_w} / {nofb_nf} + 0.29)' nrd='0.29 / {nofb_w} ' nrs='0.29 / {nofb_w} '
+ sa=0 sb=0 sd=0 mult=1 m=1
XM76 net42 nb VGND VGND sky130_fd_pr__nfet_01v8_lvt L={ni_l} W={ni_w} nf={ni_nf} ad='int(({ni_nf} + 1)/2) * {ni_w} / {ni_nf} * 0.29'
+ as='int(({ni_nf} + 2)/2) * {ni_w} / {ni_nf} * 0.29' pd='2*int(({ni_nf} + 1)/2) * ({ni_w} / {ni_nf} + 0.29)'
+ ps='2*int(({ni_nf} + 2)/2) * ({ni_w} / {ni_nf} + 0.29)' nrd='0.29 / {ni_w} ' nrs='0.29 / {ni_w} ' sa=0
+ sb=0 sd=0 mult=1 m=1
XM85 net52 pb net41 VDPWR sky130_fd_pr__pfet_01v8_lvt L={pi_l} W={pi_w} nf={pi_nf} ad='int(({pi_nf} + 1)/2) * {pi_w} / {pi_nf} * 0.29'
+ as='int(({pi_nf} + 2)/2) * {pi_w} / {pi_nf} * 0.29' pd='2*int(({pi_nf} + 1)/2) * ({pi_w} / {pi_nf} + 0.29)'
+ ps='2*int(({pi_nf} + 2)/2) * ({pi_w} / {pi_nf} + 0.29)' nrd='0.29 / {pi_w} ' nrs='0.29 / {pi_w} ' sa=0
+ sb=0 sd=0 mult={io_m} m={io_m}
XM86 net45 pcas net52 VDPWR sky130_fd_pr__pfet_01v8_lvt L={pic_l} W={pic_w} nf={pic_nf} ad='int(({pic_nf} + 1)/2) * {pic_w} / {pic_nf} * 0.29'
+ as='int(({pic_nf} + 2)/2) * {pic_w} / {pic_nf} * 0.29' pd='2*int(({pic_nf} + 1)/2) * ({pic_w} / {pic_nf} + 0.29)'
+ ps='2*int(({pic_nf} + 2)/2) * ({pic_w} / {pic_nf} + 0.29)' nrd='0.29 / {pic_w} ' nrs='0.29 / {pic_w} '
+ sa=0 sb=0 sd=0 mult={io_m} m={io_m}
XM87 net44 net51 VGND VGND sky130_fd_pr__nfet_01v8_lvt L={noi_l} W={noi_w} nf={noi_nf} ad='int(({noi_nf} + 1)/2) * {noi_w} / {noi_nf} * 0.29'
+ as='int(({noi_nf} + 2)/2) * {noi_w} / {noi_nf} * 0.29' pd='2*int(({noi_nf} + 1)/2) * ({noi_w} / {noi_nf} + 0.29)'
+ ps='2*int(({noi_nf} + 2)/2) * ({noi_w} / {noi_nf} + 0.29)' nrd='0.29 / {noi_w} ' nrs='0.29 / {noi_w} '
+ sa=0 sb=0 sd=0 mult={io_m} m={io_m}
XM62 net51 net51 VGND VGND sky130_fd_pr__nfet_01v8_lvt L={noi_l} W={noi_w} nf={noi_nf} ad='int(({noi_nf} + 1)/2) * {noi_w} / {noi_nf} * 0.29'
+ as='int(({noi_nf} + 2)/2) * {noi_w} / {noi_nf} * 0.29' pd='2*int(({noi_nf} + 1)/2) * ({noi_w} / {noi_nf} + 0.29)'
+ ps='2*int(({noi_nf} + 2)/2) * ({noi_w} / {noi_nf} + 0.29)' nrd='0.29 / {noi_w} ' nrs='0.29 / {noi_w} '
+ sa=0 sb=0 sd=0 mult=1 m=1
XM77 net51 mid net41 VDPWR sky130_fd_pr__pfet_01v8 L={poi_l} W={poi_w} nf={poi_nf} ad='int(({poi_nf} + 1)/2) * {poi_w} / {poi_nf} * 0.29'
+ as='int(({poi_nf} + 2)/2) * {poi_w} / {poi_nf} * 0.29' pd='2*int(({poi_nf} + 1)/2) * ({poi_w} / {poi_nf} + 0.29)'
+ ps='2*int(({poi_nf} + 2)/2) * ({poi_w} / {poi_nf} + 0.29)' nrd='0.29 / {poi_w} ' nrs='0.29 / {poi_w} '
+ sa=0 sb=0 sd=0 mult=1 m=1
Viout1 VDPWR net41 0
.save i(viout1)
XC2 net53 net45 sky130_fd_pr__cap_mim_m3_1 W=2 L=2 MF={c2_m} m={c2_m}
XR2 out net53 VGND sky130_fd_pr__res_xhigh_po_0p69 L={rc2_l} mult=1 m=1
XC3 net54 net44 sky130_fd_pr__cap_mim_m3_1 W=2 L=2 MF={c2_m} m={c2_m}
XR3 out net54 VGND sky130_fd_pr__res_xhigh_po_0p69 L={rc2_l} mult=1 m=1
**.ends

* expanding   symbol:  /foss/designs/ttsky26c-analog-park/xschem/bias.sym # of pins=5
** sym_path: xschem/bias.sym
** sch_path: xschem/bias.sch
.subckt bias VDPWR pIout VGND EN vbias
*.ipin EN
*.opin pIout
*.ipin VGND
*.ipin VDPWR
*.opin vbias
XM4 inm vbias VDPWR VDPWR sky130_fd_pr__pfet_01v8_lvt L=2 W=2 nf=1 ad='int((1 + 1)/2) * 2 / 1 * 0.29'
+ as='int((1 + 2)/2) * 2 / 1 * 0.29' pd='2*int((1 + 1)/2) * (2 / 1 + 0.29)' ps='2*int((1 + 2)/2) * (2 / 1 + 0.29)'
+ nrd='0.29 / 2 ' nrs='0.29 / 2 ' sa=0 sb=0 sd=0 mult=2 m=2
XM2 inp vbias VDPWR VDPWR sky130_fd_pr__pfet_01v8_lvt L=2 W=2 nf=1 ad='int((1 + 1)/2) * 2 / 1 * 0.29'
+ as='int((1 + 2)/2) * 2 / 1 * 0.29' pd='2*int((1 + 1)/2) * (2 / 1 + 0.29)' ps='2*int((1 + 2)/2) * (2 / 1 + 0.29)'
+ nrd='0.29 / 2 ' nrs='0.29 / 2 ' sa=0 sb=0 sd=0 mult=2 m=2
XM5 pIout vbias VDPWR VDPWR sky130_fd_pr__pfet_01v8_lvt L=2 W=2 nf=1 ad='int((1 + 1)/2) * 2 / 1 * 0.29'
+ as='int((1 + 2)/2) * 2 / 1 * 0.29' pd='2*int((1 + 1)/2) * (2 / 1 + 0.29)' ps='2*int((1 + 2)/2) * (2 / 1 + 0.29)'
+ nrd='0.29 / 2 ' nrs='0.29 / 2 ' sa=0 sb=0 sd=0 mult=2 m=2
XM8 inm inm VGND VGND sky130_fd_pr__nfet_01v8 L=2 W=4 nf=1 ad='int((1 + 1)/2) * 4 / 1 * 0.29' as='int((1 + 2)/2) * 4 / 1 * 0.29'
+ pd='2*int((1 + 1)/2) * (4 / 1 + 0.29)' ps='2*int((1 + 2)/2) * (4 / 1 + 0.29)' nrd='0.29 / 4 ' nrs='0.29 / 4 '
+ sa=0 sb=0 sd=0 mult=1 m=1
XM9 inp inp net1 VGND sky130_fd_pr__nfet_01v8 L=2 W=4 nf=1 ad='int((1 + 1)/2) * 4 / 1 * 0.29' as='int((1 + 2)/2) * 4 / 1 * 0.29'
+ pd='2*int((1 + 1)/2) * (4 / 1 + 0.29)' ps='2*int((1 + 2)/2) * (4 / 1 + 0.29)' nrd='0.29 / 4 ' nrs='0.29 / 4 '
+ sa=0 sb=0 sd=0 mult=4 m=4
XM10 net2 inp VGND VGND sky130_fd_pr__nfet_01v8 L=2 W=2 nf=1 ad='int((1 + 1)/2) * 2 / 1 * 0.29' as='int((1 + 2)/2) * 2 / 1 * 0.29'
+ pd='2*int((1 + 1)/2) * (2 / 1 + 0.29)' ps='2*int((1 + 2)/2) * (2 / 1 + 0.29)' nrd='0.29 / 2 ' nrs='0.29 / 2 '
+ sa=0 sb=0 sd=0 mult=2 m=2
XM11 vbias inm VGND VGND sky130_fd_pr__nfet_01v8 L=2 W=2 nf=1 ad='int((1 + 1)/2) * 2 / 1 * 0.29' as='int((1 + 2)/2) * 2 / 1 * 0.29'
+ pd='2*int((1 + 1)/2) * (2 / 1 + 0.29)' ps='2*int((1 + 2)/2) * (2 / 1 + 0.29)' nrd='0.29 / 2 ' nrs='0.29 / 2 '
+ sa=0 sb=0 sd=0 mult=2 m=2
XM15 vbias startup inm VGND sky130_fd_pr__nfet_01v8_lvt L=0.15 W=0.5 nf=1 ad='int((1 + 1)/2) * 0.5 / 1 * 0.29'
+ as='int((1 + 2)/2) * 0.5 / 1 * 0.29' pd='2*int((1 + 1)/2) * (0.5 / 1 + 0.29)' ps='2*int((1 + 2)/2) * (0.5 / 1 + 0.29)'
+ nrd='0.29 / 0.5 ' nrs='0.29 / 0.5 ' sa=0 sb=0 sd=0 mult=1 m=1
XM3 startup inm VGND VGND sky130_fd_pr__nfet_01v8 L=0.5 W=0.5 nf=1 ad='int((1 + 1)/2) * 0.5 / 1 * 0.29'
+ as='int((1 + 2)/2) * 0.5 / 1 * 0.29' pd='2*int((1 + 1)/2) * (0.5 / 1 + 0.29)' ps='2*int((1 + 2)/2) * (0.5 / 1 + 0.29)'
+ nrd='0.29 / 0.5 ' nrs='0.29 / 0.5 ' sa=0 sb=0 sd=0 mult=1 m=1
XR1 net4 net1 VGND sky130_fd_pr__res_high_po_0p69 L=6.1 mult=1 m=1
XR2 net5 net4 VGND sky130_fd_pr__res_high_po_0p69 L=6.1 mult=1 m=1
XR3 net6 net5 VGND sky130_fd_pr__res_high_po_0p69 L=6.1 mult=1 m=1
XR4 VGND net6 VGND sky130_fd_pr__res_high_po_0p69 L=6.1 mult=1 m=1
XM1 vbias net2 VDPWR VDPWR sky130_fd_pr__pfet_01v8_lvt L=2 W=2 nf=1 ad='int((1 + 1)/2) * 2 / 1 * 0.29'
+ as='int((1 + 2)/2) * 2 / 1 * 0.29' pd='2*int((1 + 1)/2) * (2 / 1 + 0.29)' ps='2*int((1 + 2)/2) * (2 / 1 + 0.29)'
+ nrd='0.29 / 2 ' nrs='0.29 / 2 ' sa=0 sb=0 sd=0 mult=2 m=2
XM12 net2 net2 VDPWR VDPWR sky130_fd_pr__pfet_01v8_lvt L=2 W=2 nf=1 ad='int((1 + 1)/2) * 2 / 1 * 0.29'
+ as='int((1 + 2)/2) * 2 / 1 * 0.29' pd='2*int((1 + 1)/2) * (2 / 1 + 0.29)' ps='2*int((1 + 2)/2) * (2 / 1 + 0.29)'
+ nrd='0.29 / 2 ' nrs='0.29 / 2 ' sa=0 sb=0 sd=0 mult=2 m=2
XM13 startup startup net3 VDPWR sky130_fd_pr__pfet_01v8_lvt L=3 W=0.42 nf=1 ad='int((1 + 1)/2) * 0.42 / 1 * 0.29'
+ as='int((1 + 2)/2) * 0.42 / 1 * 0.29' pd='2*int((1 + 1)/2) * (0.42 / 1 + 0.29)' ps='2*int((1 + 2)/2) * (0.42 / 1 + 0.29)'
+ nrd='0.29 / 0.42 ' nrs='0.29 / 0.42 ' sa=0 sb=0 sd=0 mult=1 m=1
XM16 startup nEN VGND VGND sky130_fd_pr__nfet_01v8 L=0.15 W=0.5 nf=1 ad='int((1 + 1)/2) * 0.5 / 1 * 0.29'
+ as='int((1 + 2)/2) * 0.5 / 1 * 0.29' pd='2*int((1 + 1)/2) * (0.5 / 1 + 0.29)' ps='2*int((1 + 2)/2) * (0.5 / 1 + 0.29)'
+ nrd='0.29 / 0.5 ' nrs='0.29 / 0.5 ' sa=0 sb=0 sd=0 mult=1 m=1
XM17 vbias EN VDPWR VDPWR sky130_fd_pr__pfet_01v8_hvt L=0.15 W=0.42 nf=1 ad='int((1 + 1)/2) * 0.42 / 1 * 0.29'
+ as='int((1 + 2)/2) * 0.42 / 1 * 0.29' pd='2*int((1 + 1)/2) * (0.42 / 1 + 0.29)' ps='2*int((1 + 2)/2) * (0.42 / 1 + 0.29)'
+ nrd='0.29 / 0.42 ' nrs='0.29 / 0.42 ' sa=0 sb=0 sd=0 mult=1 m=1
XM7 net3 nEN VDPWR VDPWR sky130_fd_pr__pfet_01v8_hvt L=0.15 W=0.42 nf=1 ad='int((1 + 1)/2) * 0.42 / 1 * 0.29'
+ as='int((1 + 2)/2) * 0.42 / 1 * 0.29' pd='2*int((1 + 1)/2) * (0.42 / 1 + 0.29)' ps='2*int((1 + 2)/2) * (0.42 / 1 + 0.29)'
+ nrd='0.29 / 0.42 ' nrs='0.29 / 0.42 ' sa=0 sb=0 sd=0 mult=1 m=1
XM14 VDPWR vbias VDPWR VDPWR sky130_fd_pr__pfet_01v8_lvt L=3 W=4 nf=1 ad='int((1 + 1)/2) * 4 / 1 * 0.29'
+ as='int((1 + 2)/2) * 4 / 1 * 0.29' pd='2*int((1 + 1)/2) * (4 / 1 + 0.29)' ps='2*int((1 + 2)/2) * (4 / 1 + 0.29)'
+ nrd='0.29 / 4 ' nrs='0.29 / 4 ' sa=0 sb=0 sd=0 mult=6 m=6
x1 EN VGND VGND VDPWR VDPWR nEN sky130_fd_sc_hd__inv_1
.ends

.end
